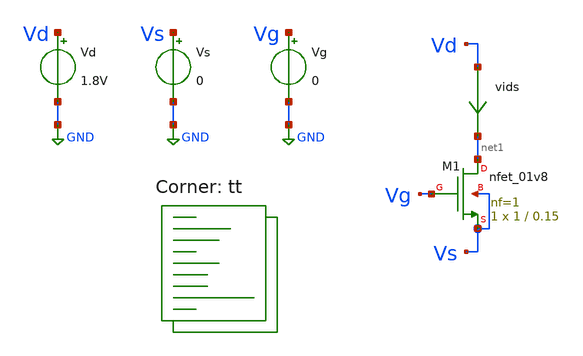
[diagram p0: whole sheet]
** sch_path: xschem/mos_curves.sch
**.subckt mos_curves
Vd Vd GND 1.8V
Vs Vs GND 0
XM1 net1 Vg Vs Vs sky130_fd_pr__nfet_01v8 L=0.15 W=1 nf=1 ad='int((nf+1)/2) * W/nf * 0.29' as='int((nf+2)/2) * W/nf * 0.29'
+ pd='2*int((nf+1)/2) * (W/nf + 0.29)' ps='2*int((nf+2)/2) * (W/nf + 0.29)' nrd='0.29 / W' nrs='0.29 / W'
+ sa=0 sb=0 sd=0 mult=1 m=1
vids Vd net1 0
.save i(vids)
Vg Vg GND 0
**** begin user architecture code
 *.lib $::SKYWATER_MODELS/sky130.lib.spice tt
.include $::SKYWATER_STDCELLS/sky130_fd_sc_hd.spice

.lib $::SKYWATER_MODELS/sky130.lib.spice tt



* ngspice commands
.options list acct opts
.control

* Go to the const plot
setplot const

echo
echo AWS Iterator = $iterator
echo

let iter_shift = 0.5
let vg_val = 0 + $iterator * $&iter_shift
let vstart = $&vg_val
let vmax = $&iter_shift + $iterator * $&iter_shift
let vdelta = 0.1
let total_runs = ceil(($&vmax - $&vg_val) / $&vdelta)
let runs = 0 + $iterator * $&total_runs
let runs_start = $&runs

* Insert vector names and set only one scale
set wr_vecnames
set wr_singlescale

* set the hcopy type
set hcopydevtype=svg


while vg_val lt $&vmax
	* Alter the voltages
	alter vg vg_val

	dc vd 0 1.8 10e-3

	set plotfile0 = plot_mos_{$&runs}_{$&vg_val}.svg
	set plottitle = run{$runs}_vgs{$&vg_val}
	hardcopy $plotfile0 i(vids) title $plottitle


	* set the iterators
	echo run $&runs
	let vg_val = vg_val + vdelta
	let runs = runs + 1

	* Destroy the transient plot to release memory
	destroy dc1

end

* switch to the const plot
setplot const

echo
echo AWS Iterator = $iterator
echo Total Runs = ($&total_runs + 1)
echo From $&vstart V to $&vmax V
echo From Run $&runs_start to $&runs
echo
.endc



**** end user architecture code
**.ends
.GLOBAL GND
.end
